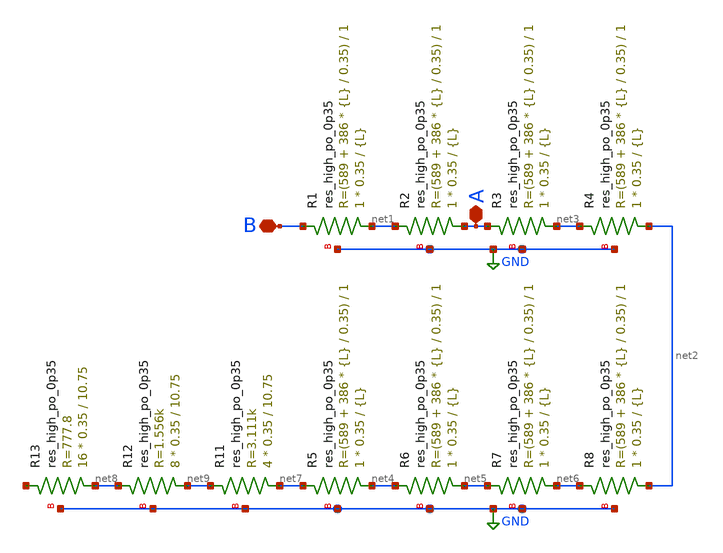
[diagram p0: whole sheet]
** sch_path: xschem/Resistor50k.sch
**.subckt Resistor50k A B
*.iopin A
*.iopin B
XR1 net1 B GND sky130_fd_pr__res_high_po_0p35 L={L} mult=1 m=1
XR2 A net1 GND sky130_fd_pr__res_high_po_0p35 L={L} mult=1 m=1
XR3 net3 A GND sky130_fd_pr__res_high_po_0p35 L={L} mult=1 m=1
XR4 net2 net3 GND sky130_fd_pr__res_high_po_0p35 L={L} mult=1 m=1
XR6 net5 net4 GND sky130_fd_pr__res_high_po_0p35 L={L} mult=1 m=1
XR7 net6 net5 GND sky130_fd_pr__res_high_po_0p35 L={L} mult=1 m=1
XR8 net2 net6 GND sky130_fd_pr__res_high_po_0p35 L={L} mult=1 m=1
XR5 net4 net7 GND sky130_fd_pr__res_high_po_0p35 L={L} mult=1 m=1
XR11 net7 net9 GND sky130_fd_pr__res_high_po_0p35 L=10.75 mult=4 m=4
XR12 net9 net8 GND sky130_fd_pr__res_high_po_0p35 L=10.75 mult=8 m=8
XR13 net8 net10 GND sky130_fd_pr__res_high_po_0p35 L=10.75 mult=16 m=16
**** begin user architecture code


.param L=4.4


**** end user architecture code
**.ends
.GLOBAL GND
.end
